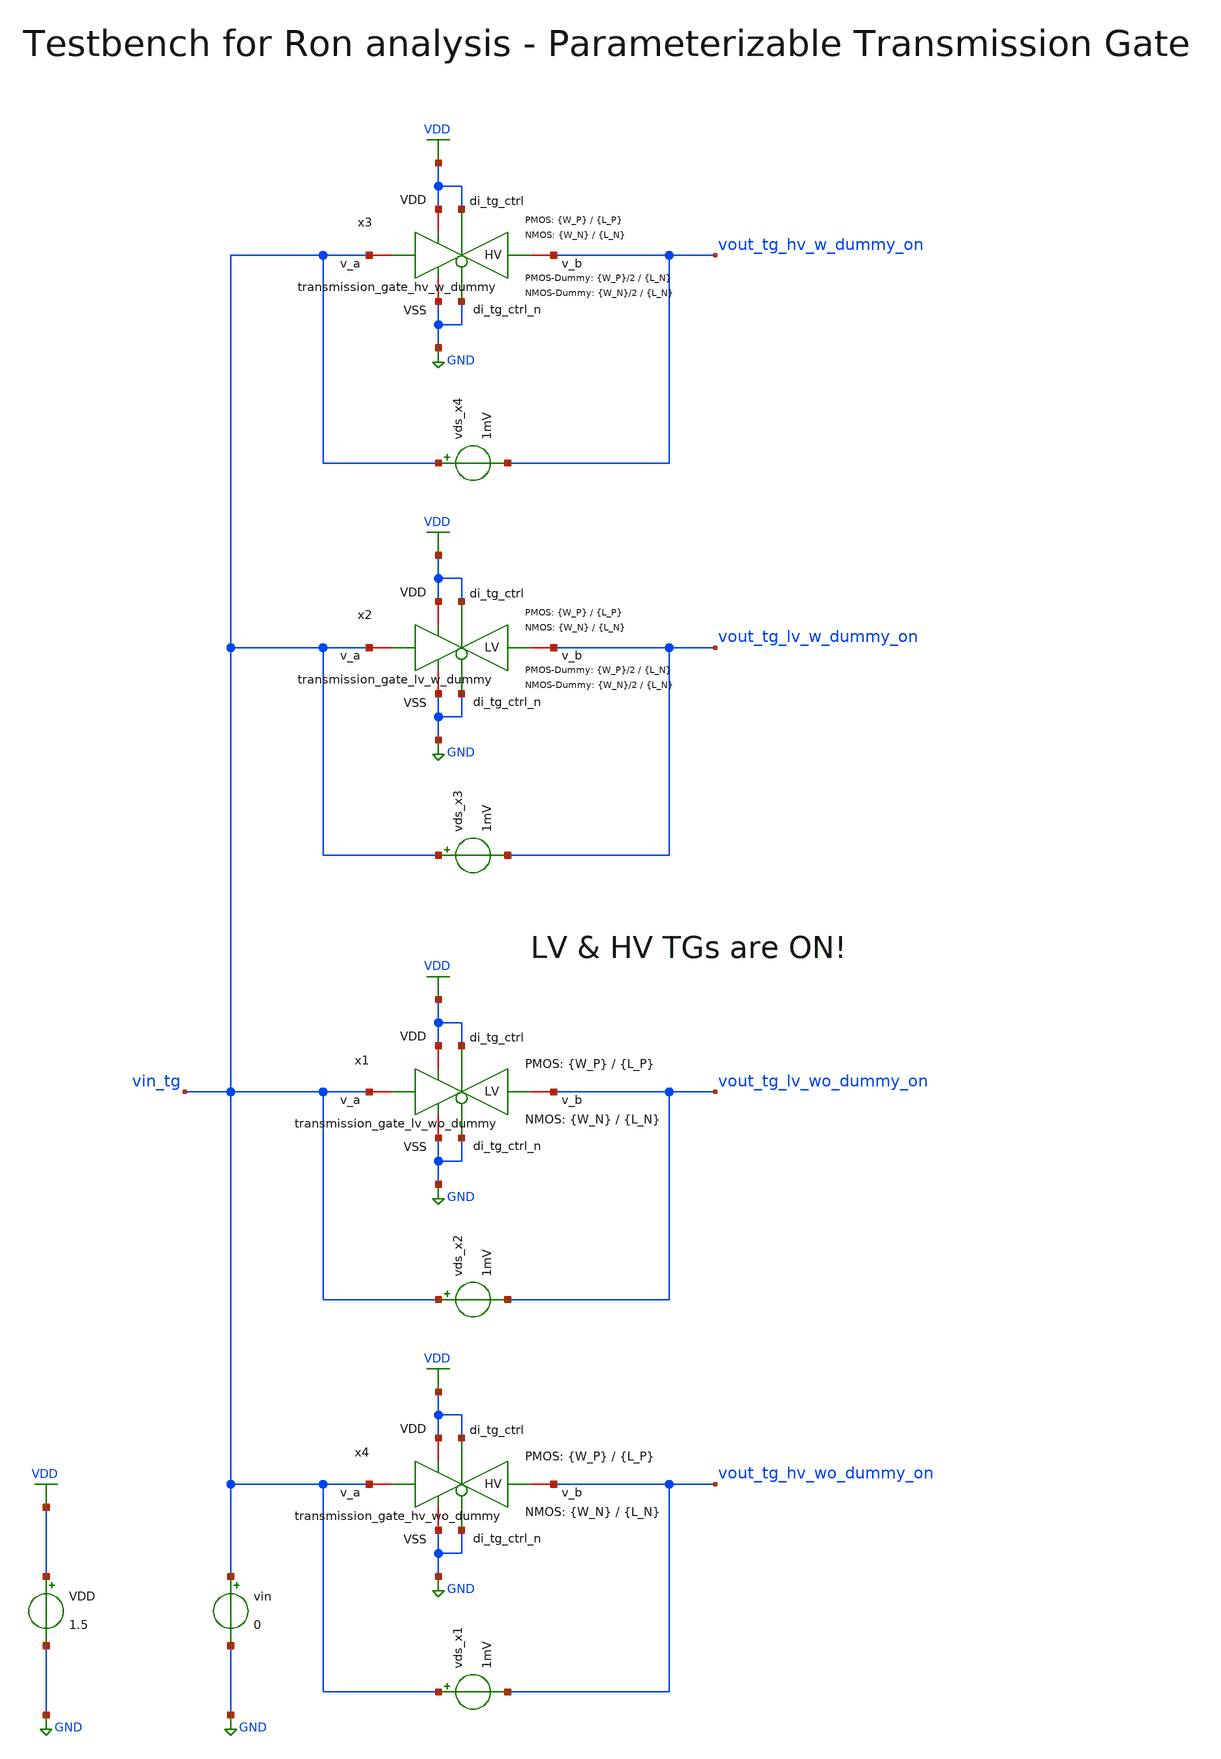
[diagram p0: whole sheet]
** sch_path: SG13G2_ATBS-ADC-main/xschem/transmission_gate/testbenches/transmission_gate_tb_dc_Ron.sch
**.subckt transmission_gate_tb_dc_Ron
VDD VDD GND 1.5
vin vin_tg GND 0
vds_x2 vin_tg vout_tg_lv_wo_dummy_on 1mV
vds_x3 vin_tg vout_tg_lv_w_dummy_on 1mV
x1 VDD VDD GND vout_tg_lv_wo_dummy_on vin_tg GND transmission_gate_lv_wo_dummy W_P={W_P} L_P={L_P} W_N={W_N}
+ L_N={L_N}
x2 VDD VDD GND vout_tg_lv_w_dummy_on vin_tg GND transmission_gate_lv_w_dummy W_P={W_P} L_P={L_P} W_N={W_N}
+ L_N={L_N} W_P_D={W_P}/2 L_P_D={L_N} W_N_D={W_N}/2 L_N_D={L_N}
vds_x4 vin_tg vout_tg_hv_w_dummy_on 1mV
vds_x1 vin_tg vout_tg_hv_wo_dummy_on 1mV
x3 VDD VDD GND vout_tg_hv_w_dummy_on vin_tg GND transmission_gate_hv_w_dummy W_P={W_P} L_P={L_P} W_N={W_N}
+ L_N={L_N} W_P_D={W_P}/2 L_P_D={L_N} W_N_D={W_N}/2 L_N_D={L_N}
x4 VDD VDD GND vout_tg_hv_wo_dummy_on vin_tg GND transmission_gate_hv_wo_dummy W_P={W_P} L_P={L_P} W_N={W_N}
+ L_N={L_N}
**** begin user architecture code

.lib cornerMOShv.lib mos_tt
.lib cornerMOSlv.lib mos_tt
.lib cornerRES.lib res_typ



.param temp=27
.param W_N=1u
.param L_N=0.50u
.param W_P=1u
.param L_P=0.50u
.options savecurrents
.control
save all

* Operating Point Analysis
op
remzerovec
write transmission_gate_tb_dc_Ron.raw
set appendwrite

* DC Sweep Analysis
dc vin 0 1.5 0.01
write transmission_gate_tb_dc_Ron.raw

* On-Resistance
* HV with Dummy
let r_hv_w_dummy_on = (v(vout_tg_hv_w_dummy_on)-v(vin_tg))/I(vds_x4)
plot r_hv_w_dummy_on xlabel 'Vin in V' ylabel 'HV Ron with Dummy in Ohm'

* LV with Dummy
let r_lv_w_dummy_on = (v(vout_tg_lv_w_dummy_on)-v(vin_tg))/I(vds_x3)
plot r_lv_w_dummy_on xlabel 'Vin in V' ylabel 'LV Ron with Dummy in Ohm'

* LV without Dummy
let r_lv_wo_dummy_on = (v(vout_tg_lv_wo_dummy_on)-v(vin_tg))/I(vds_x2)
plot r_lv_wo_dummy_on xlabel 'Vin in V' ylabel 'LV Ron without Dummy in Ohm'

* HV without Dummy
let r_hv_wo_dummy_on = (v(vout_tg_hv_wo_dummy_on)-v(vin_tg))/I(vds_x1)
plot r_hv_wo_dummy_on xlabel 'Vin in V' ylabel 'HV Ron without Dummy in Ohm'

* Writing Data
set wr_singlescale
set wr_vecnames
wrdata
+ /foss/designs/SG13G2_ATBS-ADC-main/python/plot_simulations/data/transmission_gate_tb_dc_Ron.txt v(r_hv_w_dummy_on) v(r_lv_w_dummy_on) v(r_lv_wo_dummy_on) v(r_hv_wo_dummy_on)

*quit
.endc

**** end user architecture code
**.ends

* expanding   symbol:  transmission_gate/transmission_gate_lv_wo_dummy.sym # of pins=6
** sym_path: SG13G2_ATBS-ADC-main/xschem/transmission_gate/transmission_gate_lv_wo_dummy.sym
** sch_path: SG13G2_ATBS-ADC-main/xschem/transmission_gate/transmission_gate_lv_wo_dummy.sch
.subckt transmission_gate_lv_wo_dummy VDD di_tg_ctrl VSS v_b v_a di_tg_ctrl_n  W_P=1.0u L_P=0.13u
+ W_N=1.0u L_N=0.13u
*.iopin v_a
*.iopin v_b
*.iopin VDD
*.iopin VSS
*.ipin di_tg_ctrl
*.ipin di_tg_ctrl_n
XM1 v_a di_tg_ctrl v_b VSS sg13_lv_nmos w=W_N l=L_N ng=1 m=1 mm_ok=1
XM2 v_a di_tg_ctrl_n v_b VDD sg13_lv_pmos w=W_P l=L_P ng=1 m=1 mm_ok=1
.ends


* expanding   symbol:  transmission_gate/transmission_gate_lv_w_dummy.sym # of pins=6
** sym_path: SG13G2_ATBS-ADC-main/xschem/transmission_gate/transmission_gate_lv_w_dummy.sym
** sch_path: SG13G2_ATBS-ADC-main/xschem/transmission_gate/transmission_gate_lv_w_dummy.sch
.subckt transmission_gate_lv_w_dummy VDD di_tg_ctrl VSS v_b v_a di_tg_ctrl_n  W_P=2.0u L_P=0.13u
+ W_N=2.0u L_N=0.13u W_P_D=1.0u L_P_D=0.13u W_N_D=1.0u L_N_D=0.13u
*.iopin v_a
*.iopin v_b
*.iopin VDD
*.iopin VSS
*.ipin di_tg_ctrl
*.ipin di_tg_ctrl_n
XM1 v_a di_tg_ctrl v_b VSS sg13_lv_nmos w=W_N l=L_N ng=1 m=1 mm_ok=1
XM2 v_a di_tg_ctrl_n v_b VDD sg13_lv_pmos w=W_P l=L_P ng=1 m=1 mm_ok=1
XMdummy2 v_b di_tg_ctrl v_b VDD sg13_lv_pmos w=W_P_D l=L_P_D ng=1 m=1 mm_ok=1
XMdummy1 v_b di_tg_ctrl_n v_b VSS sg13_lv_nmos w=W_N_D l=L_N_D ng=1 m=1 mm_ok=1
.ends


* expanding   symbol:  transmission_gate/transmission_gate_hv_w_dummy.sym # of pins=6
** sym_path: SG13G2_ATBS-ADC-main/xschem/transmission_gate/transmission_gate_hv_w_dummy.sym
** sch_path: SG13G2_ATBS-ADC-main/xschem/transmission_gate/transmission_gate_hv_w_dummy.sch
.subckt transmission_gate_hv_w_dummy VDD di_tg_ctrl VSS v_b v_a di_tg_ctrl_n  W_P=2.0u L_P=0.5u
+ W_N=2.0u L_N=0.5u W_P_D=1.0u L_P_D=0.5u W_N_D=1.0u L_N_D=0.5u
*.iopin v_a
*.iopin v_b
*.iopin VDD
*.iopin VSS
*.ipin di_tg_ctrl
*.ipin di_tg_ctrl_n
XM1 v_a di_tg_ctrl v_b VSS sg13_hv_nmos w=W_N l=L_N ng=1 m=1 mm_ok=1
XM2 v_a di_tg_ctrl_n v_b VDD sg13_hv_pmos w=W_P l=L_P ng=1 m=1 mm_ok=1
XMdummy1 v_b di_tg_ctrl_n v_b VSS sg13_hv_nmos w=W_N_D l=L_N_D ng=1 m=1 mm_ok=1
XMdummy2 v_b di_tg_ctrl v_b VDD sg13_hv_pmos w=W_P_D l=L_P_D ng=1 m=1 mm_ok=1
.ends


* expanding   symbol:  transmission_gate/transmission_gate_hv_wo_dummy.sym # of pins=6
** sym_path: SG13G2_ATBS-ADC-main/xschem/transmission_gate/transmission_gate_hv_wo_dummy.sym
** sch_path: SG13G2_ATBS-ADC-main/xschem/transmission_gate/transmission_gate_hv_wo_dummy.sch
.subckt transmission_gate_hv_wo_dummy VDD di_tg_ctrl VSS v_b v_a di_tg_ctrl_n  W_P=1.0u L_P=0.5u
+ W_N=1.0u L_N=0.5u
*.iopin v_a
*.iopin v_b
*.iopin VDD
*.iopin VSS
*.ipin di_tg_ctrl
*.ipin di_tg_ctrl_n
XM1 v_a di_tg_ctrl v_b VSS sg13_hv_nmos w=W_N l=L_N ng=1 m=1 mm_ok=1
XM2 v_a di_tg_ctrl_n v_b VDD sg13_hv_pmos w=W_P l=L_P ng=1 m=1 mm_ok=1
.ends

.GLOBAL GND
.GLOBAL VDD
.end
